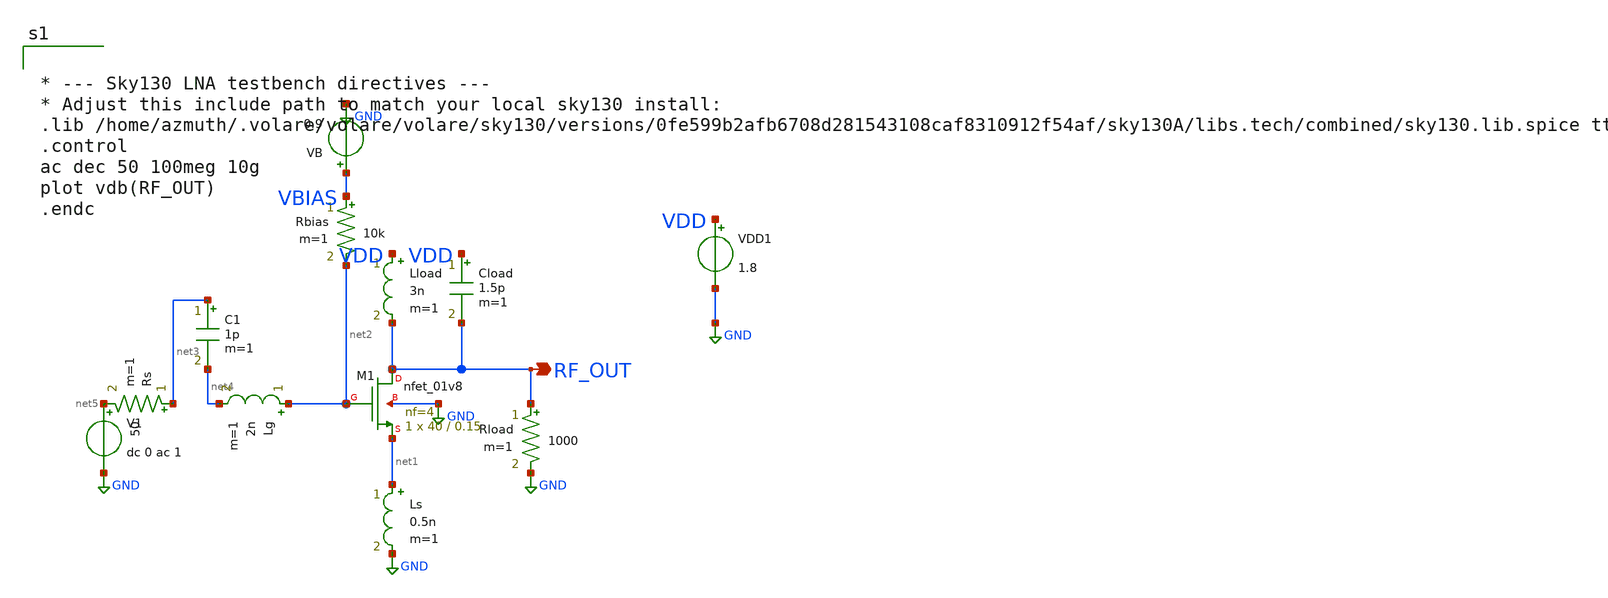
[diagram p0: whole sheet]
** sch_path: schematics/archive/lna_sky130_before_lg_sweep.sch
**.subckt lna_sky130_before_lg_sweep RF_OUT
*.opin RF_OUT
XM1 RF_OUT net2 net1 GND sky130_fd_pr__nfet_01v8 L=0.15 W=40 nf=4 ad='int((4 + 1)/2) * 40 / 4 * 0.29'
+ as='int((4 + 2)/2) * 40 / 4 * 0.29' pd='2*int((4 + 1)/2) * (40 / 4 + 0.29)' ps='2*int((4 + 2)/2) * (40 / 4 + 0.29)'
+ nrd='0.29 / 40 ' nrs='0.29 / 40 ' sa=0 sb=0 sd=0 mult=1 m=1
Lload VDD RF_OUT 3n m=1
Cload VDD RF_OUT 1.5p m=1
Ls net1 GND 0.5n m=1
Lg net2 net4 2n m=1
Rs net3 net5 50 m=1
V1 net5 GND dc 0 ac 1
Rbias VBIAS net2 10k m=1
Rload RF_OUT GND 1000 m=1
VB VBIAS GND 0.9
VDD1 VDD GND 1.8
C1 net3 net4 1p m=1
**** begin user architecture code


* --- Sky130 LNA testbench directives ---
* Adjust this include path to match your local sky130 install:
.lib /home/azmuth/.volare/volare/volare/sky130/versions/0fe599b2afb6708d281543108caf8310912f54af/sky130A/libs.tech/combined/sky130.lib.spice tt
.control
ac dec 50 100meg 10g
plot vdb(RF_OUT)
.endc


**** end user architecture code
**.ends
.GLOBAL GND
.end
